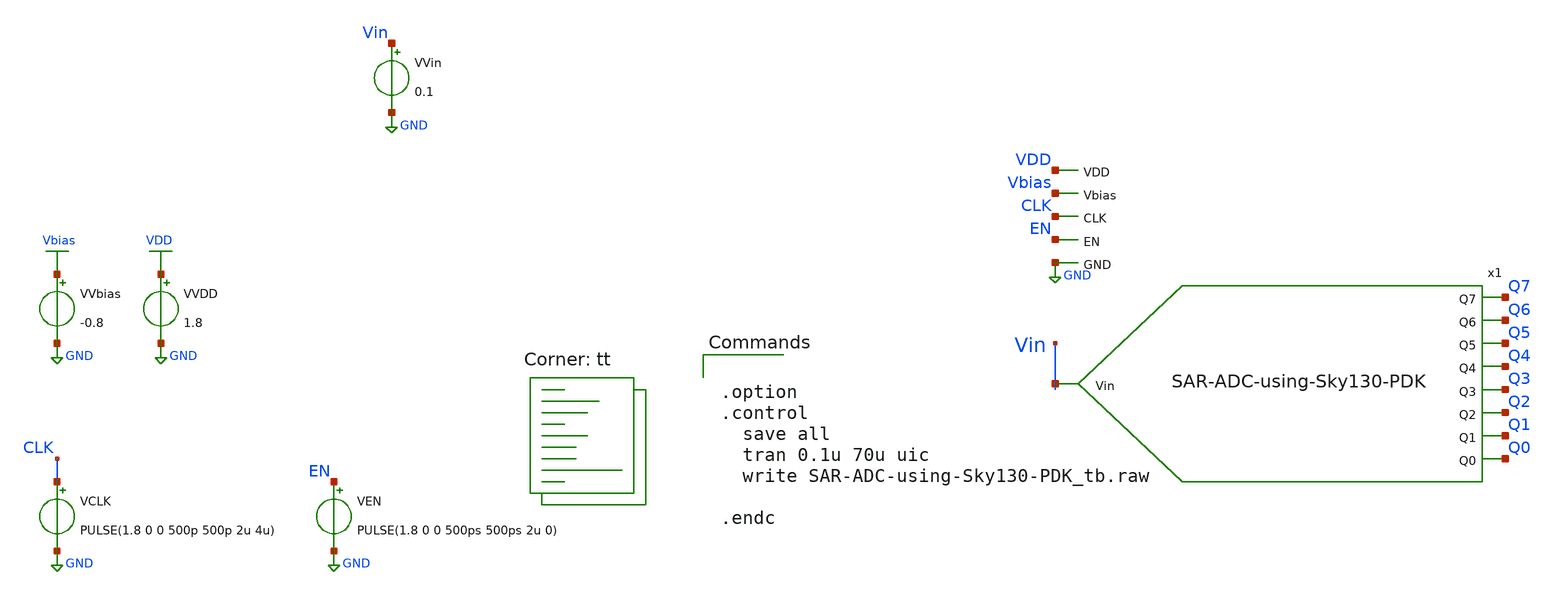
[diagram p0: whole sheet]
** sch_path: xschem/SAR-ADC-using-Sky130-PDK_tb.sch
**.subckt SAR-ADC-using-Sky130-PDK_tb
x1 VDD Vin Q0 Vbias EN Q1 CLK Q2 Q3 Q4 Q5 Q6 Q7 GND SAR-ADC-using-Sky130-PDK
VCLK CLK GND PULSE(1.8 0 0 500p 500p 2u 4u)
VVDD VDD GND 1.8
VEN EN GND PULSE(1.8 0 0 500ps 500ps 2u 0)
VVbias Vbias GND -0.8
VVin Vin GND 0.1
**** begin user architecture code


.option
.control
  save all
  tran 0.1u 70u uic
  write SAR-ADC-using-Sky130-PDK_tb.raw

.endc


.lib $::SKYWATER_MODELS/sky130.lib.spice tt
**** end user architecture code
**.ends
.GLOBAL GND
.GLOBAL VDD
.GLOBAL Vbias
.end
